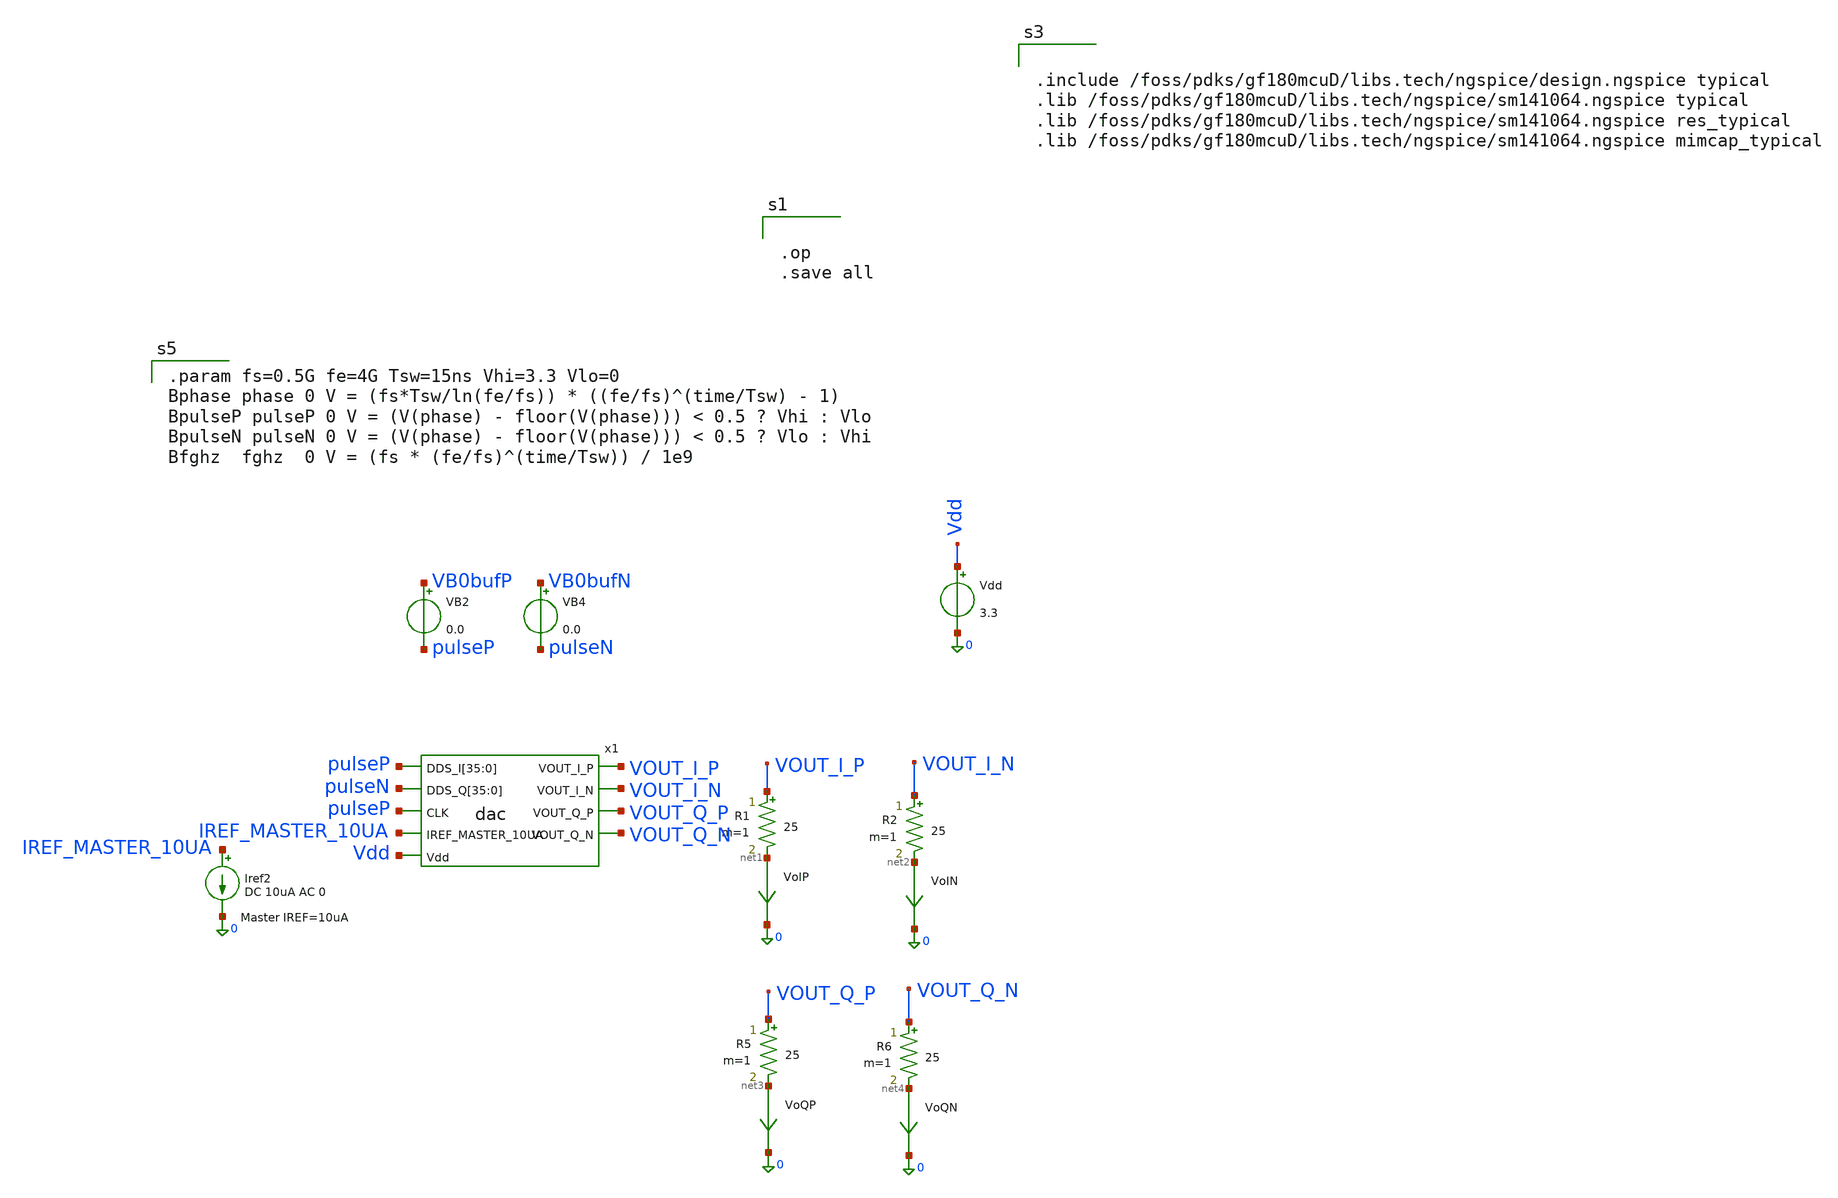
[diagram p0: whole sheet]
** sch_path: blocks/dac/test/test_dac_fsweep_10b.sch
**.subckt test_dac_fsweep_10b
Vdd Vdd 0 3.3
.save i(vdd)
VB2 VB0bufP pulseP 0.0
.save i(vb2)
VB4 VB0bufN pulseN 0.0
.save i(vb4)
x1 VOUT_I_P pulseP pulseP pulseP pulseP pulseP pulseP pulseP pulseP pulseP pulseP pulseP pulseP
+ pulseP pulseP pulseP pulseP pulseP pulseP pulseP pulseP pulseP pulseP pulseP pulseP pulseP pulseP pulseP
+ pulseP pulseP pulseP pulseP pulseP pulseP pulseP pulseP pulseP VOUT_I_N pulseN pulseN pulseN pulseN pulseN
+ pulseN pulseN pulseN pulseN pulseN pulseN pulseN pulseN pulseN pulseN pulseN pulseN pulseN pulseN pulseN
+ pulseN pulseN pulseN pulseN pulseN pulseN pulseN pulseN pulseN pulseN pulseN pulseN pulseN pulseN pulseN
+ pulseN pulseP VOUT_Q_P IREF_MASTER_10UA VOUT_Q_N Vdd dac
Iref2 IREF_MASTER_10UA 0 DC 10uA AC 0
R1 VOUT_I_P net1 25 m=1
R2 VOUT_I_N net2 25 m=1
VoIP net1 0 0
.save i(voip)
VoIN net2 0 0
.save i(voin)
R5 VOUT_Q_P net3 25 m=1
R6 VOUT_Q_N net4 25 m=1
VoQP net3 0 0
.save i(voqp)
VoQN net4 0 0
.save i(voqn)
**** begin user architecture code



.save all
.control

tran 1p 2ns
* plot VU1syncP+6 VU1syncN+6 VU2syncP+6 VU2syncN+6 VgN+12 VgP Dm ClkP+18 ClkN+18 i(Vl1)*5E4-6
*+ i(Vl2)*5E4-6 (i(Vl1)-i(Vl2))*5E4-12
* plot ClkP+6 ClkN+6 VU0in VB1in VU0syncP-6 VU0syncN-12 VB1syncP-6 VB1syncN-12
* plot Vout1P+15E-3 Vout1N+15E-3 Vout1P-Vout1N
plot ClkP+5 ClkN+5 VB3bufP-5 VB3bufN-5 x1.Vg1P-10 x1.Vg1N-10 x2.Vg1P-15 x2.Vg1N-15

plot i(VoutB3P)-i(VoutB3N) i(VoutU0P)-i(VoutU0N) i(VoutB4P)-i(VoutB4N) i(VoutB2P)-i(VoutB2N)
+ i(VoutB1P)-i(VoutB1N)

*plot VB1syncP VB1syncN-6 VB4syncN-6 VU0bufP-12 VB1bufP-12 VB4bufP-12 VU0bufN-18 VB1bufN-18
*+ VB4bufN-18

let diff = i(Vl1)-i(Vl2)
let imax = 630E-6
plot pulseP {diff/{imax}}*5 fghz

plot VoutP VoutN pulseP+5 pulseN+5

plot i(Vl1)-i(Vl2) imax fghz*100E-6

plot i(Vdd) ylimit -0.1 0.1

* plot i(VoutB3P)+100E-6 i(VoutB3N)+100E-6 i(VoutB3P)-i(VoutB3N) i(VoutB3N)+i(VoutB3P)
*+ i(v.x1.Vcrr1)-200E-6 i(v.x1.Vcrr2)-200E-6
* plot i(Vl1) VB1in/5E4+200E-6 VU0in/5E4+200E-6
* wrdata /foss/designs/dds/dac_isource_unary_pmos_80ua_v4_tt_500ps.csv ClkP ClkN Din VdsyncP VdsyncN
*+ i(Vl1) i(Vl2)
.endc





.op
.save all



.param fs=0.5G fe=4G Tsw=15ns Vhi=3.3 Vlo=0
Bphase phase 0 V = (fs*Tsw/ln(fe/fs)) * ((fe/fs)^(time/Tsw) - 1)
BpulseP pulseP 0 V = (V(phase) - floor(V(phase))) < 0.5 ? Vhi : Vlo
BpulseN pulseN 0 V = (V(phase) - floor(V(phase))) < 0.5 ? Vlo : Vhi
Bfghz  fghz  0 V = (fs * (fe/fs)^(time/Tsw)) / 1e9





.include /foss/pdks/gf180mcuD/libs.tech/ngspice/design.ngspice typical
.lib /foss/pdks/gf180mcuD/libs.tech/ngspice/sm141064.ngspice typical
.lib /foss/pdks/gf180mcuD/libs.tech/ngspice/sm141064.ngspice res_typical
.lib /foss/pdks/gf180mcuD/libs.tech/ngspice/sm141064.ngspice mimcap_typical


**** end user architecture code
**.ends
.end
